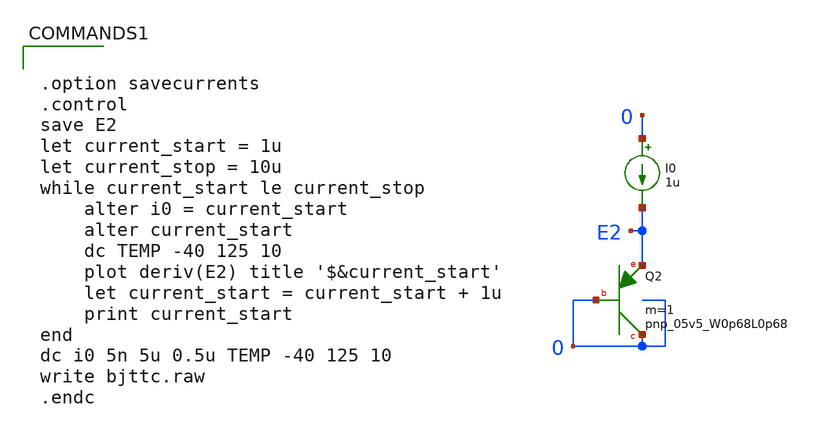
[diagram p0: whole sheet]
** sch_path: custom_gds/tt_um_bgr_agolmanesh/xschem/bjttc.sch
**.subckt bjttc
XQ2 0 0 E2 sky130_fd_pr__pnp_05v5_W0p68L0p68 m=1
I0 0 E2 1u
**** begin user architecture code


.option savecurrents
.control
save E2
let current_start = 1u
let current_stop = 10u
while current_start le current_stop
    alter i0 = current_start
    alter current_start
    dc TEMP -40 125 10
    plot deriv(E2) title '$&current_start'
    let current_start = current_start + 1u
    print current_start
end
dc i0 5n 5u 0.5u TEMP -40 125 10
write bjttc.raw
.endc



** opencircuitdesign pdks install
.lib $::SKYWATER_MODELS/sky130.lib.spice tt


**** end user architecture code
**.ends
.end
